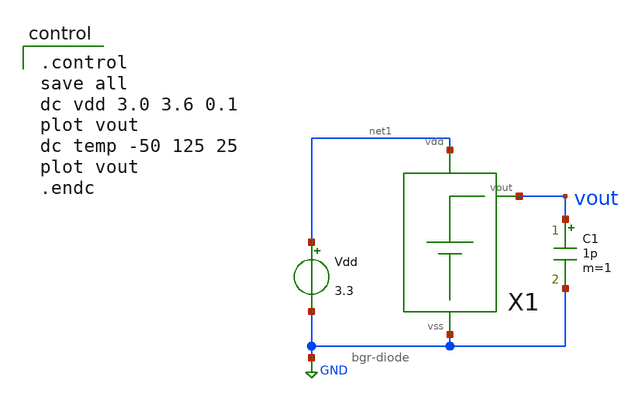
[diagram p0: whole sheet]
** sch_path: BGR/xschem/tb-dc_bgr-diode.sch
**.subckt tb-dc_bgr-diode
Vdd net1 GND 3.3
X1 GND net1 vout bgr-diode
C1 vout GND 1p m=1
**** begin user architecture code

.include $::180MCU_MODELS/design.ngspice
.lib $::180MCU_MODELS/sm141064.ngspice typical
.lib $::180MCU_MODELS/sm141064.ngspice res_typical
.lib $::180MCU_MODELS/sm141064.ngspice moscap_typical
.lib $::180MCU_MODELS/sm141064.ngspice bjt_typical
* .lib $::180MCU_MODELS/sm141064.ngspice res_statistical


.control
save all
dc vdd 3.0 3.6 0.1
plot vout
dc temp -50 125 25
plot vout
.endc

**** end user architecture code
**.ends
.GLOBAL GND
.end
